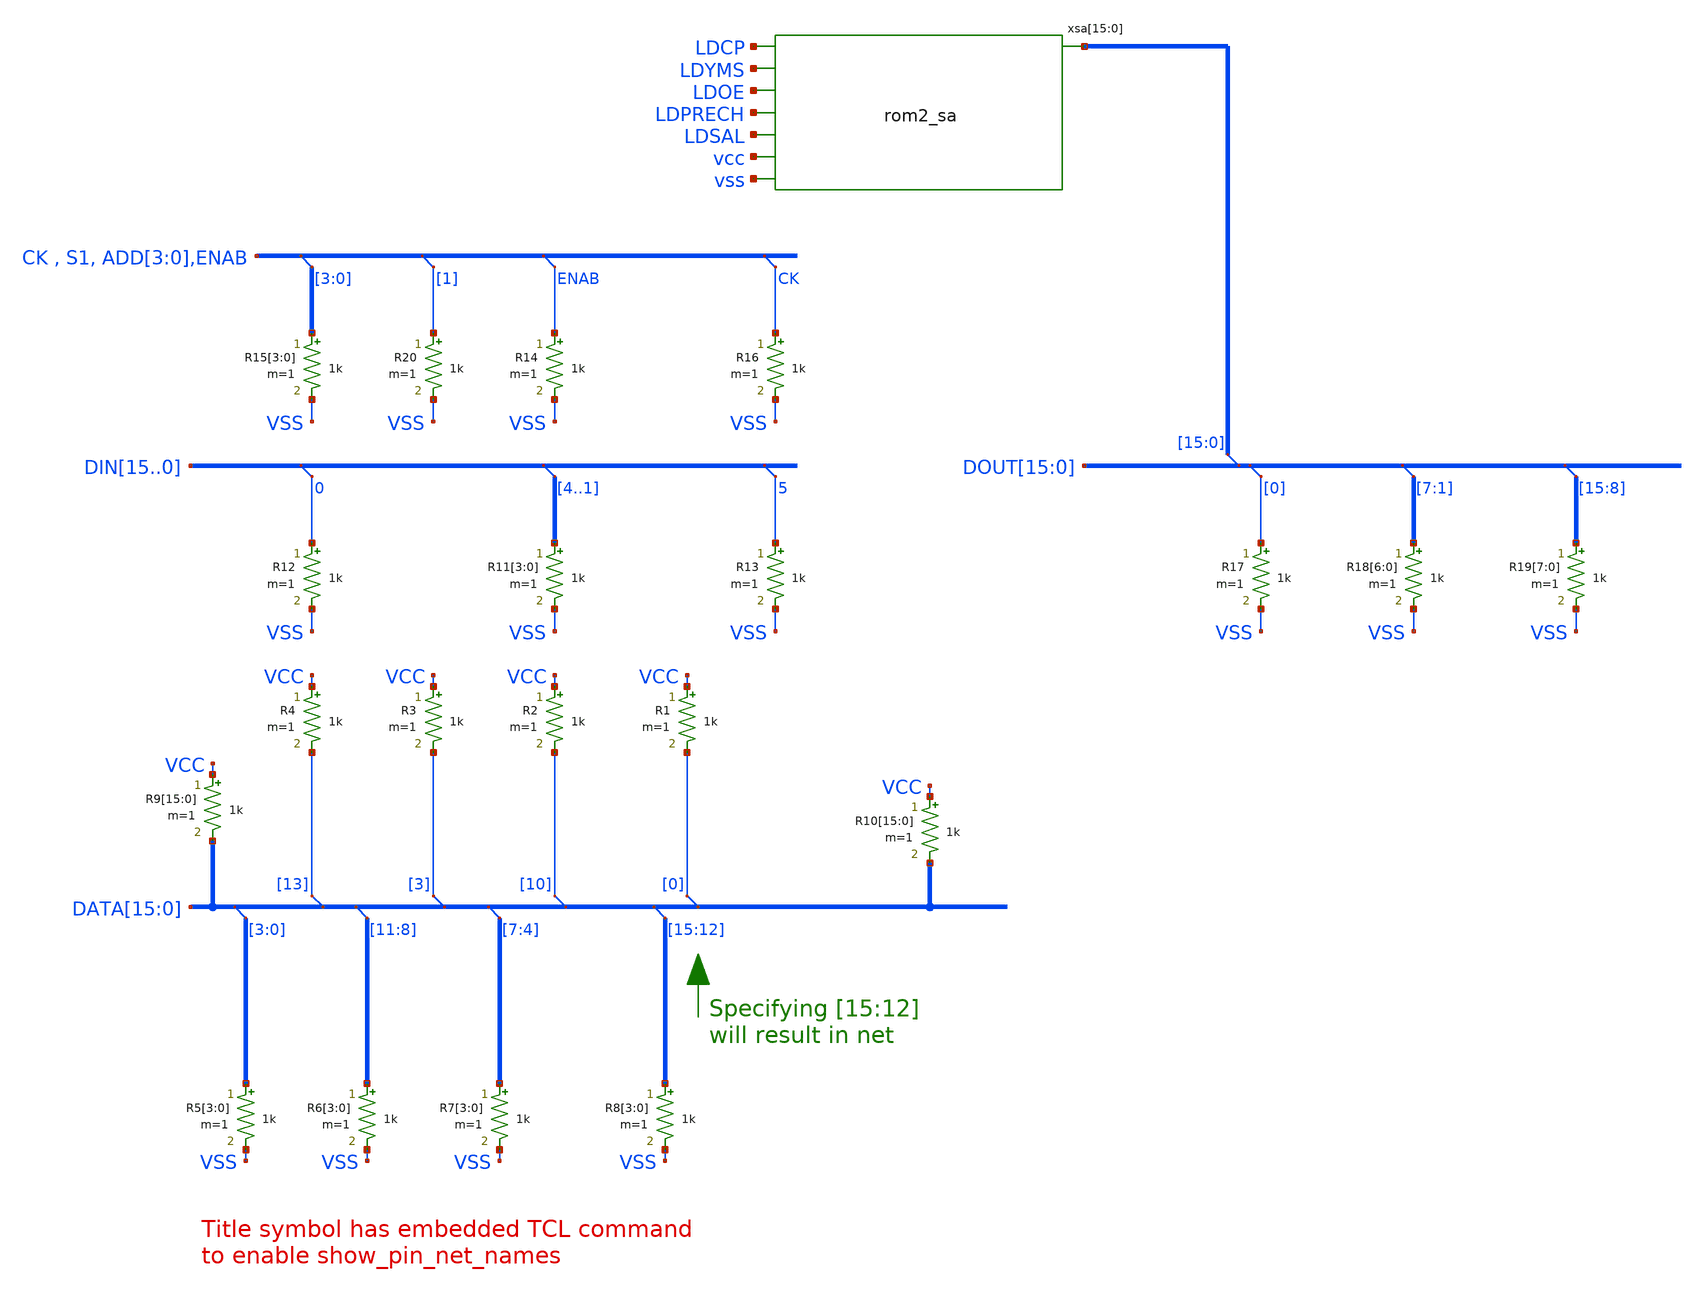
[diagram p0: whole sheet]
** sch_path: tests/test_sweep_diff/examples/test_bus_tap/schematic/test_bus_tap.sch
* Copyright (C) 1998-2024 Stefan Frederik Schippers
* This program is free software; you can redistribute it and/or modify
* it under the terms of the GNU General Public License as published by
* the Free Software Foundation; either version 2 of the License, or
* (at your option) any later version.
* This program is distributed in the hope that it will be useful,
* but WITHOUT ANY WARRANTY; without even the implied warranty of
* MERCHANTABILITY or FITNESS FOR A PARTICULAR PURPOSE.  See the
* GNU General Public License for more details.
* You should have received a copy of the GNU General Public License
* along with this program; if not, write to the Free Software
**.subckt test_bus_tap
* tap: DATA[15:0] --> DATA[3]
* tap: DATA[15:0] --> DATA[13]
* tap: DATA[15:0] --> DATA[7:4]
* tap: DATA[15:0] --> DATA[11:8]
* tap: DATA[15:0] --> DATA[3:0]
* tap: DATA[15:0] --> DATA[10]
* tap: DATA[15:0] --> DATA[0]
R1 VCC DATA[0] 1k m=1
R2 VCC DATA[10] 1k m=1
R3 VCC DATA[3] 1k m=1
R4 VCC DATA[13] 1k m=1
R5[3] DATA[3] VSS 1k m=1
R5[2] DATA[2] VSS 1k m=1
R5[1] DATA[1] VSS 1k m=1
R5[0] DATA[0] VSS 1k m=1
R6[3] DATA[11] VSS 1k m=1
R6[2] DATA[10] VSS 1k m=1
R6[1] DATA[9] VSS 1k m=1
R6[0] DATA[8] VSS 1k m=1
R7[3] DATA[7] VSS 1k m=1
R7[2] DATA[6] VSS 1k m=1
R7[1] DATA[5] VSS 1k m=1
R7[0] DATA[4] VSS 1k m=1
R8[3] DATA[15] VSS 1k m=1
R8[2] DATA[14] VSS 1k m=1
R8[1] DATA[13] VSS 1k m=1
R8[0] DATA[12] VSS 1k m=1
* tap: DATA[15:0] --> DATA[15:12]
R9[15] VCC DATA[15] 1k m=1
R9[14] VCC DATA[14] 1k m=1
R9[13] VCC DATA[13] 1k m=1
R9[12] VCC DATA[12] 1k m=1
R9[11] VCC DATA[11] 1k m=1
R9[10] VCC DATA[10] 1k m=1
R9[9] VCC DATA[9] 1k m=1
R9[8] VCC DATA[8] 1k m=1
R9[7] VCC DATA[7] 1k m=1
R9[6] VCC DATA[6] 1k m=1
R9[5] VCC DATA[5] 1k m=1
R9[4] VCC DATA[4] 1k m=1
R9[3] VCC DATA[3] 1k m=1
R9[2] VCC DATA[2] 1k m=1
R9[1] VCC DATA[1] 1k m=1
R9[0] VCC DATA[0] 1k m=1
R10[15] VCC DATA[15] 1k m=1
R10[14] VCC DATA[14] 1k m=1
R10[13] VCC DATA[13] 1k m=1
R10[12] VCC DATA[12] 1k m=1
R10[11] VCC DATA[11] 1k m=1
R10[10] VCC DATA[10] 1k m=1
R10[9] VCC DATA[9] 1k m=1
R10[8] VCC DATA[8] 1k m=1
R10[7] VCC DATA[7] 1k m=1
R10[6] VCC DATA[6] 1k m=1
R10[5] VCC DATA[5] 1k m=1
R10[4] VCC DATA[4] 1k m=1
R10[3] VCC DATA[3] 1k m=1
R10[2] VCC DATA[2] 1k m=1
R10[1] VCC DATA[1] 1k m=1
R10[0] VCC DATA[0] 1k m=1
* tap: DIN[15..0] --> DIN0
* tap: DIN[15..0] --> DIN[4..1]
R11[3] DIN4 VSS 1k m=1
R11[2] DIN3 VSS 1k m=1
R11[1] DIN2 VSS 1k m=1
R11[0] DIN1 VSS 1k m=1
R12 DIN0 VSS 1k m=1
* tap: DIN[15..0] --> DIN5
R13 DIN5 VSS 1k m=1
* tap: CK , S1, ADD[3:0],ENAB --> ADD[3:0]
* tap: CK , S1, ADD[3:0],ENAB --> ENAB
R15[3] ADD[3] VSS 1k m=1
R15[2] ADD[2] VSS 1k m=1
R15[1] ADD[1] VSS 1k m=1
R15[0] ADD[0] VSS 1k m=1
R14 ENAB VSS 1k m=1
* tap: CK , S1, ADD[3:0],ENAB --> CK
R16 CK VSS 1k m=1
* tap: DOUT[15:0] --> DOUT[0]
* tap: DOUT[15:0] --> DOUT[7:1]
R18[6] DOUT[7] VSS 1k m=1
R18[5] DOUT[6] VSS 1k m=1
R18[4] DOUT[5] VSS 1k m=1
R18[3] DOUT[4] VSS 1k m=1
R18[2] DOUT[3] VSS 1k m=1
R18[1] DOUT[2] VSS 1k m=1
R18[0] DOUT[1] VSS 1k m=1
R17 DOUT[0] VSS 1k m=1
* tap: DOUT[15:0] --> DOUT[15:8]
R19[7] DOUT[15] VSS 1k m=1
R19[6] DOUT[14] VSS 1k m=1
R19[5] DOUT[13] VSS 1k m=1
R19[4] DOUT[12] VSS 1k m=1
R19[3] DOUT[11] VSS 1k m=1
R19[2] DOUT[10] VSS 1k m=1
R19[1] DOUT[9] VSS 1k m=1
R19[0] DOUT[8] VSS 1k m=1
xsa[15] DOUT[15] LDCP LDYMS LDOE LDPRECH LDSAL vcc vss rom2_sa
xsa[14] DOUT[14] LDCP LDYMS LDOE LDPRECH LDSAL vcc vss rom2_sa
xsa[13] DOUT[13] LDCP LDYMS LDOE LDPRECH LDSAL vcc vss rom2_sa
xsa[12] DOUT[12] LDCP LDYMS LDOE LDPRECH LDSAL vcc vss rom2_sa
xsa[11] DOUT[11] LDCP LDYMS LDOE LDPRECH LDSAL vcc vss rom2_sa
xsa[10] DOUT[10] LDCP LDYMS LDOE LDPRECH LDSAL vcc vss rom2_sa
xsa[9] DOUT[9] LDCP LDYMS LDOE LDPRECH LDSAL vcc vss rom2_sa
xsa[8] DOUT[8] LDCP LDYMS LDOE LDPRECH LDSAL vcc vss rom2_sa
xsa[7] DOUT[7] LDCP LDYMS LDOE LDPRECH LDSAL vcc vss rom2_sa
xsa[6] DOUT[6] LDCP LDYMS LDOE LDPRECH LDSAL vcc vss rom2_sa
xsa[5] DOUT[5] LDCP LDYMS LDOE LDPRECH LDSAL vcc vss rom2_sa
xsa[4] DOUT[4] LDCP LDYMS LDOE LDPRECH LDSAL vcc vss rom2_sa
xsa[3] DOUT[3] LDCP LDYMS LDOE LDPRECH LDSAL vcc vss rom2_sa
xsa[2] DOUT[2] LDCP LDYMS LDOE LDPRECH LDSAL vcc vss rom2_sa
xsa[1] DOUT[1] LDCP LDYMS LDOE LDPRECH LDSAL vcc vss rom2_sa
xsa[0] DOUT[0] LDCP LDYMS LDOE LDPRECH LDSAL vcc vss rom2_sa
* tap: DOUT[15:0] --> DOUT[15:0]
* tap: CK , S1, ADD[3:0],ENAB --> ADD[1]
R20 ADD[1] VSS 1k m=1
**.ends
.end
